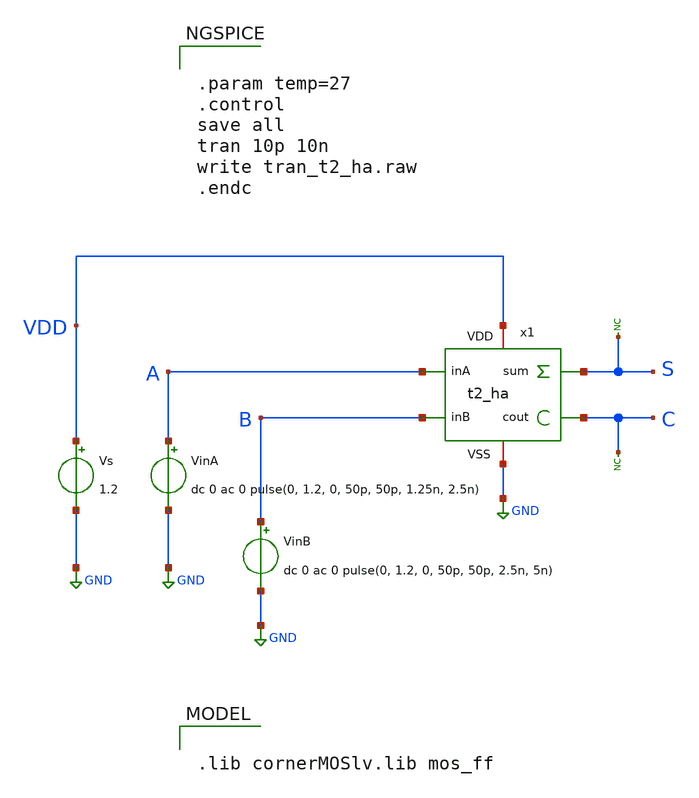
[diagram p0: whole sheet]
** sch_path: Team 2 Design/design_data/xschem/t2_ha_tb.sch
**.subckt t2_ha_tb
x1 VDD GND A B S C t2_ha
VinA A GND dc 0 ac 0 pulse(0, 1.2, 0, 50p, 50p, 1.25n, 2.5n)
VinB B GND dc 0 ac 0 pulse(0, 1.2, 0, 50p, 50p, 2.5n, 5n)
Vs VDD GND 1.2
* noconn S
* noconn C
**** begin user architecture code


.param temp=27
.control
save all
tran 10p 10n
write tran_t2_ha.raw
.endc



.lib cornerMOSlv.lib mos_ff

**** end user architecture code
**.ends
.GLOBAL GND
.end
